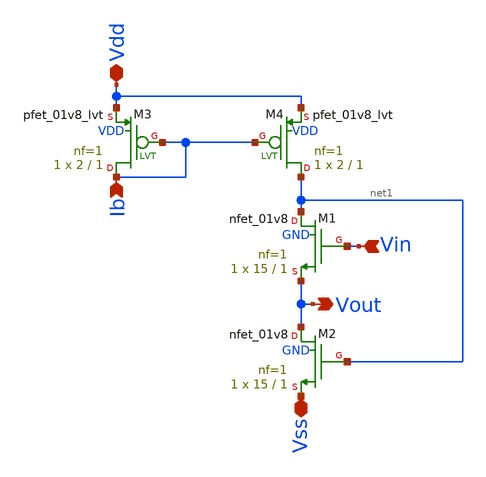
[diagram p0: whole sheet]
** sch_path: xschem/fvf.sch
**.subckt fvf Vin Ib Vout Vdd Vss
*.ipin Vin
*.ipin Ib
*.opin Vout
*.iopin Vdd
*.iopin Vss
XM1 net1 Vin Vout GND sky130_fd_pr__nfet_01v8 L=1 W=15 nf=1 ad='int((nf+1)/2) * W/nf * 0.29' as='int((nf+2)/2) * W/nf * 0.29'
+ pd='2*int((nf+1)/2) * (W/nf + 0.29)' ps='2*int((nf+2)/2) * (W/nf + 0.29)' nrd='0.29 / W' nrs='0.29 / W'
+ sa=0 sb=0 sd=0 mult=1 m=1
XM2 Vout net1 Vss GND sky130_fd_pr__nfet_01v8 L=1 W=15 nf=1 ad='int((nf+1)/2) * W/nf * 0.29' as='int((nf+2)/2) * W/nf * 0.29'
+ pd='2*int((nf+1)/2) * (W/nf + 0.29)' ps='2*int((nf+2)/2) * (W/nf + 0.29)' nrd='0.29 / W' nrs='0.29 / W'
+ sa=0 sb=0 sd=0 mult=1 m=1
XM3 Ib Ib Vdd VDD sky130_fd_pr__pfet_01v8_lvt L=1 W=2 nf=1 ad='int((nf+1)/2) * W/nf * 0.29' as='int((nf+2)/2) * W/nf * 0.29'
+ pd='2*int((nf+1)/2) * (W/nf + 0.29)' ps='2*int((nf+2)/2) * (W/nf + 0.29)' nrd='0.29 / W' nrs='0.29 / W'
+ sa=0 sb=0 sd=0 mult=1 m=1
XM4 net1 Ib Vdd VDD sky130_fd_pr__pfet_01v8_lvt L=1 W=2 nf=1 ad='int((nf+1)/2) * W/nf * 0.29' as='int((nf+2)/2) * W/nf * 0.29'
+ pd='2*int((nf+1)/2) * (W/nf + 0.29)' ps='2*int((nf+2)/2) * (W/nf + 0.29)' nrd='0.29 / W' nrs='0.29 / W'
+ sa=0 sb=0 sd=0 mult=1 m=1
**.ends
.end
